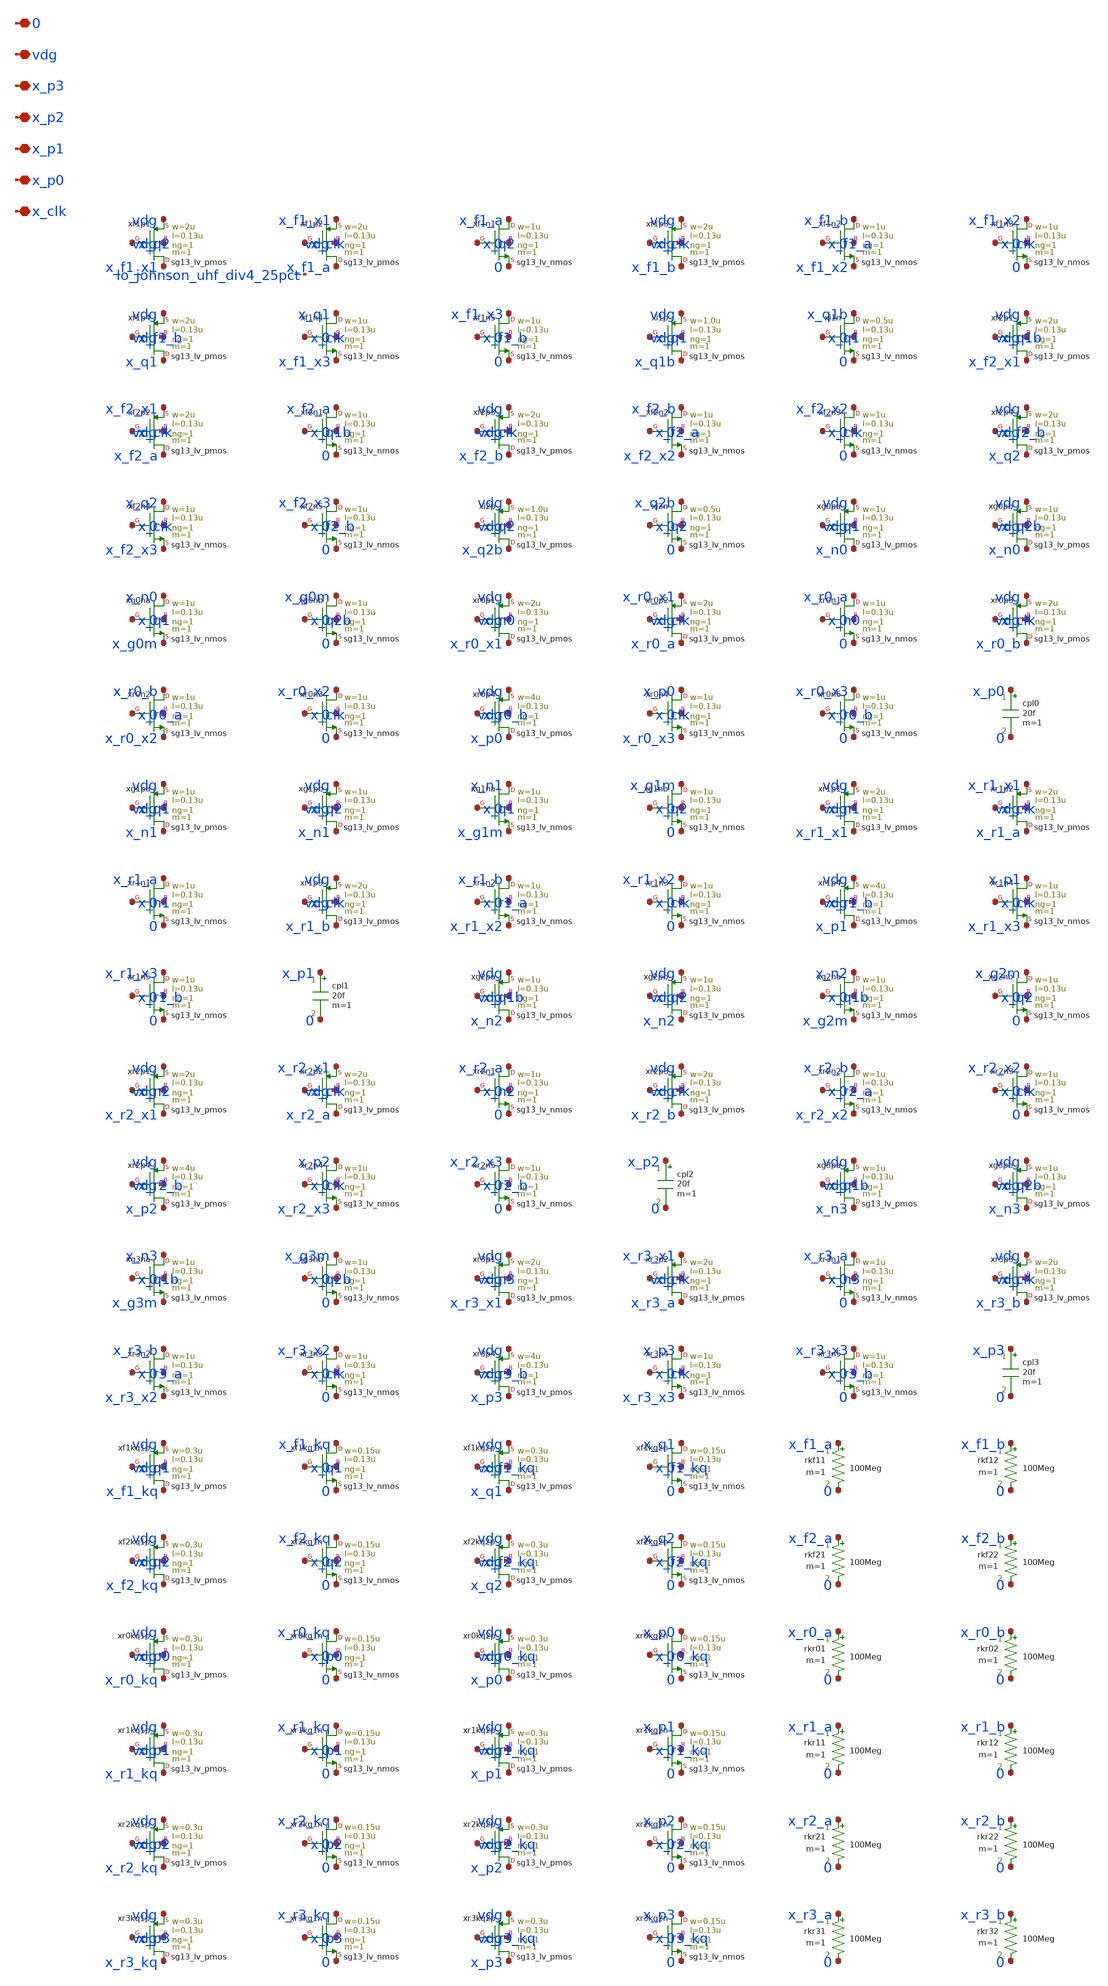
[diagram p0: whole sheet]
** sch_path: analog/lo/sch/lo_johnson_uhf.sch
**.subckt lo_johnson_uhf x_clk x_p0 x_p1 x_p2 x_p3 vdg 0
*.iopin x_clk
*.iopin x_p0
*.iopin x_p1
*.iopin x_p2
*.iopin x_p3
*.iopin vdg
*.iopin 0
Xxf1p1 x_f1_x1 x_q2 vdg vdg sg13_lv_pmos w=2u l=0.13u ng=1 m=1 mm_ok=1
Xxf1p2 x_f1_a x_clk x_f1_x1 vdg sg13_lv_pmos w=2u l=0.13u ng=1 m=1 mm_ok=1
Xxf1n1 x_f1_a x_q2 0 0 sg13_lv_nmos w=1u l=0.13u ng=1 m=1 mm_ok=1
Xxf1p3 x_f1_b x_clk vdg vdg sg13_lv_pmos w=2u l=0.13u ng=1 m=1 mm_ok=1
Xxf1n2 x_f1_b x_f1_a x_f1_x2 0 sg13_lv_nmos w=1u l=0.13u ng=1 m=1 mm_ok=1
Xxf1n3 x_f1_x2 x_clk 0 0 sg13_lv_nmos w=1u l=0.13u ng=1 m=1 mm_ok=1
Xxf1p4 x_q1 x_f1_b vdg vdg sg13_lv_pmos w=2u l=0.13u ng=1 m=1 mm_ok=1
Xxf1n4 x_q1 x_clk x_f1_x3 0 sg13_lv_nmos w=1u l=0.13u ng=1 m=1 mm_ok=1
Xxf1n5 x_f1_x3 x_f1_b 0 0 sg13_lv_nmos w=1u l=0.13u ng=1 m=1 mm_ok=1
Xxi1p x_q1b x_q1 vdg vdg sg13_lv_pmos w=1.0u l=0.13u ng=1 m=1 mm_ok=1
Xxi1n x_q1b x_q1 0 0 sg13_lv_nmos w=0.5u l=0.13u ng=1 m=1 mm_ok=1
Xxf2p1 x_f2_x1 x_q1b vdg vdg sg13_lv_pmos w=2u l=0.13u ng=1 m=1 mm_ok=1
Xxf2p2 x_f2_a x_clk x_f2_x1 vdg sg13_lv_pmos w=2u l=0.13u ng=1 m=1 mm_ok=1
Xxf2n1 x_f2_a x_q1b 0 0 sg13_lv_nmos w=1u l=0.13u ng=1 m=1 mm_ok=1
Xxf2p3 x_f2_b x_clk vdg vdg sg13_lv_pmos w=2u l=0.13u ng=1 m=1 mm_ok=1
Xxf2n2 x_f2_b x_f2_a x_f2_x2 0 sg13_lv_nmos w=1u l=0.13u ng=1 m=1 mm_ok=1
Xxf2n3 x_f2_x2 x_clk 0 0 sg13_lv_nmos w=1u l=0.13u ng=1 m=1 mm_ok=1
Xxf2p4 x_q2 x_f2_b vdg vdg sg13_lv_pmos w=2u l=0.13u ng=1 m=1 mm_ok=1
Xxf2n4 x_q2 x_clk x_f2_x3 0 sg13_lv_nmos w=1u l=0.13u ng=1 m=1 mm_ok=1
Xxf2n5 x_f2_x3 x_f2_b 0 0 sg13_lv_nmos w=1u l=0.13u ng=1 m=1 mm_ok=1
Xxi2p x_q2b x_q2 vdg vdg sg13_lv_pmos w=1.0u l=0.13u ng=1 m=1 mm_ok=1
Xxi2n x_q2b x_q2 0 0 sg13_lv_nmos w=0.5u l=0.13u ng=1 m=1 mm_ok=1
Xxg0pa x_n0 x_q1 vdg vdg sg13_lv_pmos w=1u l=0.13u ng=1 m=1 mm_ok=1
Xxg0pb x_n0 x_q2b vdg vdg sg13_lv_pmos w=1u l=0.13u ng=1 m=1 mm_ok=1
Xxg0na x_n0 x_q1 x_g0m 0 sg13_lv_nmos w=1u l=0.13u ng=1 m=1 mm_ok=1
Xxg0nb x_g0m x_q2b 0 0 sg13_lv_nmos w=1u l=0.13u ng=1 m=1 mm_ok=1
Xxr0p1 x_r0_x1 x_n0 vdg vdg sg13_lv_pmos w=2u l=0.13u ng=1 m=1 mm_ok=1
Xxr0p2 x_r0_a x_clk x_r0_x1 vdg sg13_lv_pmos w=2u l=0.13u ng=1 m=1 mm_ok=1
Xxr0n1 x_r0_a x_n0 0 0 sg13_lv_nmos w=1u l=0.13u ng=1 m=1 mm_ok=1
Xxr0p3 x_r0_b x_clk vdg vdg sg13_lv_pmos w=2u l=0.13u ng=1 m=1 mm_ok=1
Xxr0n2 x_r0_b x_r0_a x_r0_x2 0 sg13_lv_nmos w=1u l=0.13u ng=1 m=1 mm_ok=1
Xxr0n3 x_r0_x2 x_clk 0 0 sg13_lv_nmos w=1u l=0.13u ng=1 m=1 mm_ok=1
Xxr0p4 x_p0 x_r0_b vdg vdg sg13_lv_pmos w=4u l=0.13u ng=1 m=1 mm_ok=1
Xxr0n4 x_p0 x_clk x_r0_x3 0 sg13_lv_nmos w=1u l=0.13u ng=1 m=1 mm_ok=1
Xxr0n5 x_r0_x3 x_r0_b 0 0 sg13_lv_nmos w=1u l=0.13u ng=1 m=1 mm_ok=1
cpl0 x_p0 0 20f m=1
Xxg1pa x_n1 x_q1 vdg vdg sg13_lv_pmos w=1u l=0.13u ng=1 m=1 mm_ok=1
Xxg1pb x_n1 x_q2 vdg vdg sg13_lv_pmos w=1u l=0.13u ng=1 m=1 mm_ok=1
Xxg1na x_n1 x_q1 x_g1m 0 sg13_lv_nmos w=1u l=0.13u ng=1 m=1 mm_ok=1
Xxg1nb x_g1m x_q2 0 0 sg13_lv_nmos w=1u l=0.13u ng=1 m=1 mm_ok=1
Xxr1p1 x_r1_x1 x_n1 vdg vdg sg13_lv_pmos w=2u l=0.13u ng=1 m=1 mm_ok=1
Xxr1p2 x_r1_a x_clk x_r1_x1 vdg sg13_lv_pmos w=2u l=0.13u ng=1 m=1 mm_ok=1
Xxr1n1 x_r1_a x_n1 0 0 sg13_lv_nmos w=1u l=0.13u ng=1 m=1 mm_ok=1
Xxr1p3 x_r1_b x_clk vdg vdg sg13_lv_pmos w=2u l=0.13u ng=1 m=1 mm_ok=1
Xxr1n2 x_r1_b x_r1_a x_r1_x2 0 sg13_lv_nmos w=1u l=0.13u ng=1 m=1 mm_ok=1
Xxr1n3 x_r1_x2 x_clk 0 0 sg13_lv_nmos w=1u l=0.13u ng=1 m=1 mm_ok=1
Xxr1p4 x_p1 x_r1_b vdg vdg sg13_lv_pmos w=4u l=0.13u ng=1 m=1 mm_ok=1
Xxr1n4 x_p1 x_clk x_r1_x3 0 sg13_lv_nmos w=1u l=0.13u ng=1 m=1 mm_ok=1
Xxr1n5 x_r1_x3 x_r1_b 0 0 sg13_lv_nmos w=1u l=0.13u ng=1 m=1 mm_ok=1
cpl1 x_p1 0 20f m=1
Xxg2pa x_n2 x_q1b vdg vdg sg13_lv_pmos w=1u l=0.13u ng=1 m=1 mm_ok=1
Xxg2pb x_n2 x_q2 vdg vdg sg13_lv_pmos w=1u l=0.13u ng=1 m=1 mm_ok=1
Xxg2na x_n2 x_q1b x_g2m 0 sg13_lv_nmos w=1u l=0.13u ng=1 m=1 mm_ok=1
Xxg2nb x_g2m x_q2 0 0 sg13_lv_nmos w=1u l=0.13u ng=1 m=1 mm_ok=1
Xxr2p1 x_r2_x1 x_n2 vdg vdg sg13_lv_pmos w=2u l=0.13u ng=1 m=1 mm_ok=1
Xxr2p2 x_r2_a x_clk x_r2_x1 vdg sg13_lv_pmos w=2u l=0.13u ng=1 m=1 mm_ok=1
Xxr2n1 x_r2_a x_n2 0 0 sg13_lv_nmos w=1u l=0.13u ng=1 m=1 mm_ok=1
Xxr2p3 x_r2_b x_clk vdg vdg sg13_lv_pmos w=2u l=0.13u ng=1 m=1 mm_ok=1
Xxr2n2 x_r2_b x_r2_a x_r2_x2 0 sg13_lv_nmos w=1u l=0.13u ng=1 m=1 mm_ok=1
Xxr2n3 x_r2_x2 x_clk 0 0 sg13_lv_nmos w=1u l=0.13u ng=1 m=1 mm_ok=1
Xxr2p4 x_p2 x_r2_b vdg vdg sg13_lv_pmos w=4u l=0.13u ng=1 m=1 mm_ok=1
Xxr2n4 x_p2 x_clk x_r2_x3 0 sg13_lv_nmos w=1u l=0.13u ng=1 m=1 mm_ok=1
Xxr2n5 x_r2_x3 x_r2_b 0 0 sg13_lv_nmos w=1u l=0.13u ng=1 m=1 mm_ok=1
cpl2 x_p2 0 20f m=1
Xxg3pa x_n3 x_q1b vdg vdg sg13_lv_pmos w=1u l=0.13u ng=1 m=1 mm_ok=1
Xxg3pb x_n3 x_q2b vdg vdg sg13_lv_pmos w=1u l=0.13u ng=1 m=1 mm_ok=1
Xxg3na x_n3 x_q1b x_g3m 0 sg13_lv_nmos w=1u l=0.13u ng=1 m=1 mm_ok=1
Xxg3nb x_g3m x_q2b 0 0 sg13_lv_nmos w=1u l=0.13u ng=1 m=1 mm_ok=1
Xxr3p1 x_r3_x1 x_n3 vdg vdg sg13_lv_pmos w=2u l=0.13u ng=1 m=1 mm_ok=1
Xxr3p2 x_r3_a x_clk x_r3_x1 vdg sg13_lv_pmos w=2u l=0.13u ng=1 m=1 mm_ok=1
Xxr3n1 x_r3_a x_n3 0 0 sg13_lv_nmos w=1u l=0.13u ng=1 m=1 mm_ok=1
Xxr3p3 x_r3_b x_clk vdg vdg sg13_lv_pmos w=2u l=0.13u ng=1 m=1 mm_ok=1
Xxr3n2 x_r3_b x_r3_a x_r3_x2 0 sg13_lv_nmos w=1u l=0.13u ng=1 m=1 mm_ok=1
Xxr3n3 x_r3_x2 x_clk 0 0 sg13_lv_nmos w=1u l=0.13u ng=1 m=1 mm_ok=1
Xxr3p4 x_p3 x_r3_b vdg vdg sg13_lv_pmos w=4u l=0.13u ng=1 m=1 mm_ok=1
Xxr3n4 x_p3 x_clk x_r3_x3 0 sg13_lv_nmos w=1u l=0.13u ng=1 m=1 mm_ok=1
Xxr3n5 x_r3_x3 x_r3_b 0 0 sg13_lv_nmos w=1u l=0.13u ng=1 m=1 mm_ok=1
cpl3 x_p3 0 20f m=1
Xxf1kq1p x_f1_kq x_q1 vdg vdg sg13_lv_pmos w=0.3u l=0.13u ng=1 m=1 mm_ok=1
Xxf1kq1n x_f1_kq x_q1 0 0 sg13_lv_nmos w=0.15u l=0.13u ng=1 m=1 mm_ok=1
Xxf1kq2p x_q1 x_f1_kq vdg vdg sg13_lv_pmos w=0.3u l=0.13u ng=1 m=1 mm_ok=1
Xxf1kq2n x_q1 x_f1_kq 0 0 sg13_lv_nmos w=0.15u l=0.13u ng=1 m=1 mm_ok=1
rkf11 x_f1_a 0 100Meg m=1
rkf12 x_f1_b 0 100Meg m=1
Xxf2kq1p x_f2_kq x_q2 vdg vdg sg13_lv_pmos w=0.3u l=0.13u ng=1 m=1 mm_ok=1
Xxf2kq1n x_f2_kq x_q2 0 0 sg13_lv_nmos w=0.15u l=0.13u ng=1 m=1 mm_ok=1
Xxf2kq2p x_q2 x_f2_kq vdg vdg sg13_lv_pmos w=0.3u l=0.13u ng=1 m=1 mm_ok=1
Xxf2kq2n x_q2 x_f2_kq 0 0 sg13_lv_nmos w=0.15u l=0.13u ng=1 m=1 mm_ok=1
rkf21 x_f2_a 0 100Meg m=1
rkf22 x_f2_b 0 100Meg m=1
Xxr0kq1p x_r0_kq x_p0 vdg vdg sg13_lv_pmos w=0.3u l=0.13u ng=1 m=1 mm_ok=1
Xxr0kq1n x_r0_kq x_p0 0 0 sg13_lv_nmos w=0.15u l=0.13u ng=1 m=1 mm_ok=1
Xxr0kq2p x_p0 x_r0_kq vdg vdg sg13_lv_pmos w=0.3u l=0.13u ng=1 m=1 mm_ok=1
Xxr0kq2n x_p0 x_r0_kq 0 0 sg13_lv_nmos w=0.15u l=0.13u ng=1 m=1 mm_ok=1
rkr01 x_r0_a 0 100Meg m=1
rkr02 x_r0_b 0 100Meg m=1
Xxr1kq1p x_r1_kq x_p1 vdg vdg sg13_lv_pmos w=0.3u l=0.13u ng=1 m=1 mm_ok=1
Xxr1kq1n x_r1_kq x_p1 0 0 sg13_lv_nmos w=0.15u l=0.13u ng=1 m=1 mm_ok=1
Xxr1kq2p x_p1 x_r1_kq vdg vdg sg13_lv_pmos w=0.3u l=0.13u ng=1 m=1 mm_ok=1
Xxr1kq2n x_p1 x_r1_kq 0 0 sg13_lv_nmos w=0.15u l=0.13u ng=1 m=1 mm_ok=1
rkr11 x_r1_a 0 100Meg m=1
rkr12 x_r1_b 0 100Meg m=1
Xxr2kq1p x_r2_kq x_p2 vdg vdg sg13_lv_pmos w=0.3u l=0.13u ng=1 m=1 mm_ok=1
Xxr2kq1n x_r2_kq x_p2 0 0 sg13_lv_nmos w=0.15u l=0.13u ng=1 m=1 mm_ok=1
Xxr2kq2p x_p2 x_r2_kq vdg vdg sg13_lv_pmos w=0.3u l=0.13u ng=1 m=1 mm_ok=1
Xxr2kq2n x_p2 x_r2_kq 0 0 sg13_lv_nmos w=0.15u l=0.13u ng=1 m=1 mm_ok=1
rkr21 x_r2_a 0 100Meg m=1
rkr22 x_r2_b 0 100Meg m=1
Xxr3kq1p x_r3_kq x_p3 vdg vdg sg13_lv_pmos w=0.3u l=0.13u ng=1 m=1 mm_ok=1
Xxr3kq1n x_r3_kq x_p3 0 0 sg13_lv_nmos w=0.15u l=0.13u ng=1 m=1 mm_ok=1
Xxr3kq2p x_p3 x_r3_kq vdg vdg sg13_lv_pmos w=0.3u l=0.13u ng=1 m=1 mm_ok=1
Xxr3kq2n x_p3 x_r3_kq 0 0 sg13_lv_nmos w=0.15u l=0.13u ng=1 m=1 mm_ok=1
rkr31 x_r3_a 0 100Meg m=1
rkr32 x_r3_b 0 100Meg m=1
**.ends
.end
